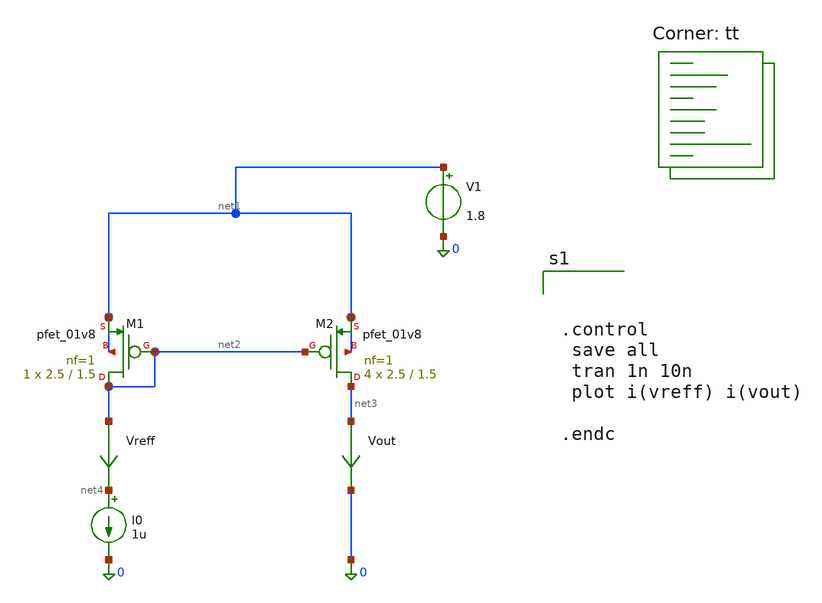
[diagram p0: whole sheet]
** sch_path: Training-3/cth_tugas.sch
**.subckt cth_tugas
XM1 net2 net2 net1 net1 sky130_fd_pr__pfet_01v8 L=1.5 W=2.5 nf=1 ad='int((nf+1)/2) * W/nf * 0.29' as='int((nf+2)/2) * W/nf * 0.29'
+ pd='2*int((nf+1)/2) * (W/nf + 0.29)' ps='2*int((nf+2)/2) * (W/nf + 0.29)' nrd='0.29 / W' nrs='0.29 / W'
+ sa=0 sb=0 sd=0 mult=1 m=1
XM2 net3 net2 net1 net1 sky130_fd_pr__pfet_01v8 L=1.5 W=2.5 nf=1 ad='int((nf+1)/2) * W/nf * 0.29' as='int((nf+2)/2) * W/nf * 0.29'
+ pd='2*int((nf+1)/2) * (W/nf + 0.29)' ps='2*int((nf+2)/2) * (W/nf + 0.29)' nrd='0.29 / W' nrs='0.29 / W'
+ sa=0 sb=0 sd=0 mult=4 m=4
V1 net1 0 1.8
Vreff net2 net4 0
.save i(vreff)
Vout net3 0 0
.save i(vout)
I0 net4 0 1u
**** begin user architecture code
.lib $::SKYWATER_MODELS/sky130.lib.spice tt



.control
 save all
 tran 1n 10n
 plot i(vreff) i(vout)

.endc



**** end user architecture code
**.ends
.end
